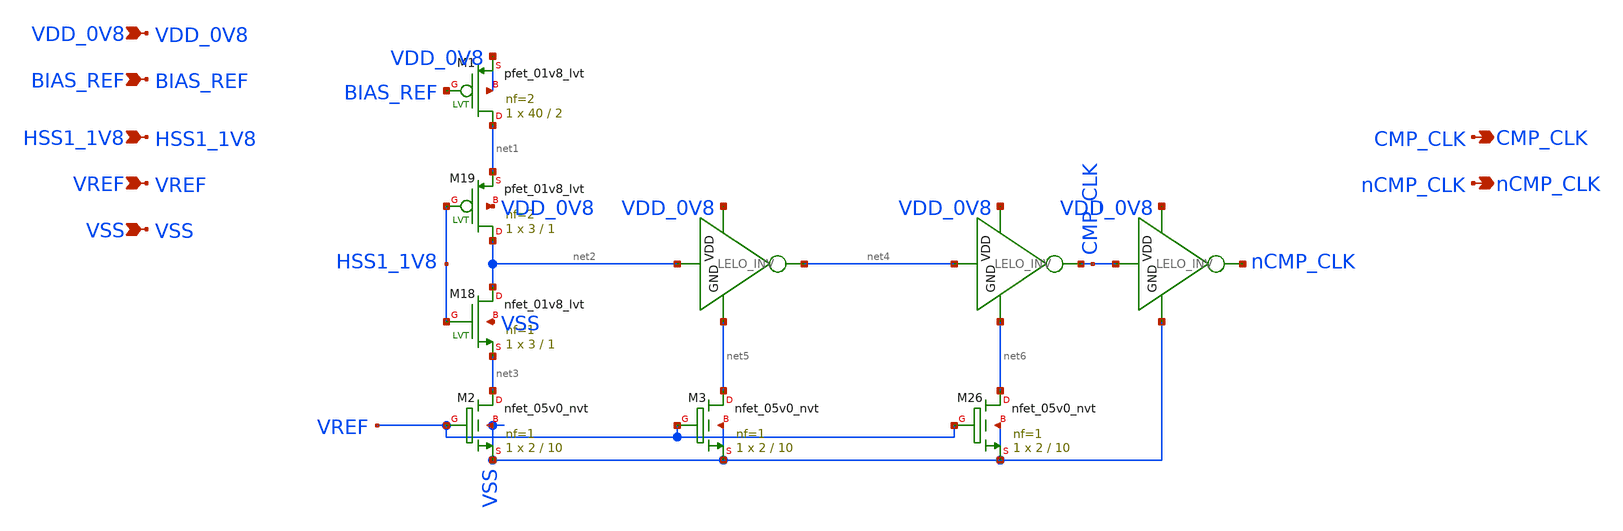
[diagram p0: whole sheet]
** sch_path: design/LELO_SVOD_SKY130A/PVT_DELAY.sch
**.subckt PVT_DELAY VDD_0V8 HSS1_1V8 VREF VSS CMP_CLK nCMP_CLK BIAS_REF
*.ipin VDD_0V8
*.ipin HSS1_1V8
*.ipin VREF
*.ipin VSS
*.opin CMP_CLK
*.opin nCMP_CLK
*.ipin BIAS_REF
XM18 net2 HSS1_1V8 net3 VSS sky130_fd_pr__nfet_01v8_lvt L=1 W=3 nf=1 ad='int((1 + 1)/2) * 3 / 1 * 0.29'
+ as='int((1 + 2)/2) * 3 / 1 * 0.29' pd='2*int((1 + 1)/2) * (3 / 1 + 0.29)' ps='2*int((1 + 2)/2) * (3 / 1 + 0.29)'
+ nrd='0.29 / 3 ' nrs='0.29 / 3 ' sa=0 sb=0 sd=0 mult=1 m=1
XM1 net1 BIAS_REF VDD_0V8 VDD_0V8 sky130_fd_pr__pfet_01v8_lvt L=2 W=40 nf=2 ad='int((2 + 1)/2) * 40 / 2 * 0.29'
+ as='int((2 + 2)/2) * 40 / 2 * 0.29' pd='2*int((2 + 1)/2) * (40 / 2 + 0.29)' ps='2*int((2 + 2)/2) * (40 / 2 + 0.29)'
+ nrd='0.29 / 40 ' nrs='0.29 / 40 ' sa=0 sb=0 sd=0 mult=1 m=1
XM19 net2 HSS1_1V8 net1 VDD_0V8 sky130_fd_pr__pfet_01v8_lvt L=1 W=3 nf=2 ad='int((2 + 1)/2) * 3 / 2 * 0.29'
+ as='int((2 + 2)/2) * 3 / 2 * 0.29' pd='2*int((2 + 1)/2) * (3 / 2 + 0.29)' ps='2*int((2 + 2)/2) * (3 / 2 + 0.29)'
+ nrd='0.29 / 3 ' nrs='0.29 / 3 ' sa=0 sb=0 sd=0 mult=1 m=1
x7 VDD_0V8 net2 net4 net5 LELO_INV
x8 VDD_0V8 net4 CMP_CLK net6 LELO_INV
XM2 net3 VREF VSS VSS sky130_fd_pr__nfet_05v0_nvt L=10 W=2 nf=1 ad='int((1 + 1)/2) * 2 / 1 * 0.29' as='int((1 + 2)/2) * 2 / 1 * 0.29'
+ pd='2*int((1 + 1)/2) * (2 / 1 + 0.29)' ps='2*int((1 + 2)/2) * (2 / 1 + 0.29)' nrd='0.29 / 2 ' nrs='0.29 / 2 '
+ sa=0 sb=0 sd=0 mult=1 m=1
XM3 net5 VREF VSS VSS sky130_fd_pr__nfet_05v0_nvt L=10 W=2 nf=1 ad='int((1 + 1)/2) * 2 / 1 * 0.29' as='int((1 + 2)/2) * 2 / 1 * 0.29'
+ pd='2*int((1 + 1)/2) * (2 / 1 + 0.29)' ps='2*int((1 + 2)/2) * (2 / 1 + 0.29)' nrd='0.29 / 2 ' nrs='0.29 / 2 '
+ sa=0 sb=0 sd=0 mult=1 m=1
XM26 net6 VREF VSS VSS sky130_fd_pr__nfet_05v0_nvt L=10 W=2 nf=1 ad='int((1 + 1)/2) * 2 / 1 * 0.29' as='int((1 + 2)/2) * 2 / 1 * 0.29'
+ pd='2*int((1 + 1)/2) * (2 / 1 + 0.29)' ps='2*int((1 + 2)/2) * (2 / 1 + 0.29)' nrd='0.29 / 2 ' nrs='0.29 / 2 '
+ sa=0 sb=0 sd=0 mult=1 m=1
x5 VDD_0V8 CMP_CLK nCMP_CLK VSS LELO_INV
**.ends

* expanding   symbol:  LELO_SVOD_SKY130A/LELO_INV.sym # of pins=4
** sym_path: design/LELO_SVOD_SKY130A/LELO_INV.sym
** sch_path: design/LELO_SVOD_SKY130A/LELO_INV.sch
.subckt LELO_INV VDD VIN VOUT GND
*.ipin VIN
*.ipin VDD
*.ipin GND
*.opin VOUT
XM1 VOUT VIN GND GND sky130_fd_pr__nfet_01v8_lvt L=0.15 W=1 nf=1 ad='int((1 + 1)/2) * 1 / 1 * 0.29' as='int((1 + 2)/2) * 1 / 1 * 0.29'
+ pd='2*int((1 + 1)/2) * (1 / 1 + 0.29)' ps='2*int((1 + 2)/2) * (1 / 1 + 0.29)' nrd='0.29 / 1 ' nrs='0.29 / 1 '
+ sa=0 sb=0 sd=0 mult=1 m=1
XM2 VOUT VIN VDD VDD sky130_fd_pr__pfet_01v8_lvt L=0.35 W=1 nf=1 ad='int((1 + 1)/2) * 1 / 1 * 0.29' as='int((1 + 2)/2) * 1 / 1 * 0.29'
+ pd='2*int((1 + 1)/2) * (1 / 1 + 0.29)' ps='2*int((1 + 2)/2) * (1 / 1 + 0.29)' nrd='0.29 / 1 ' nrs='0.29 / 1 '
+ sa=0 sb=0 sd=0 mult=2 m=2
.ends

.end
